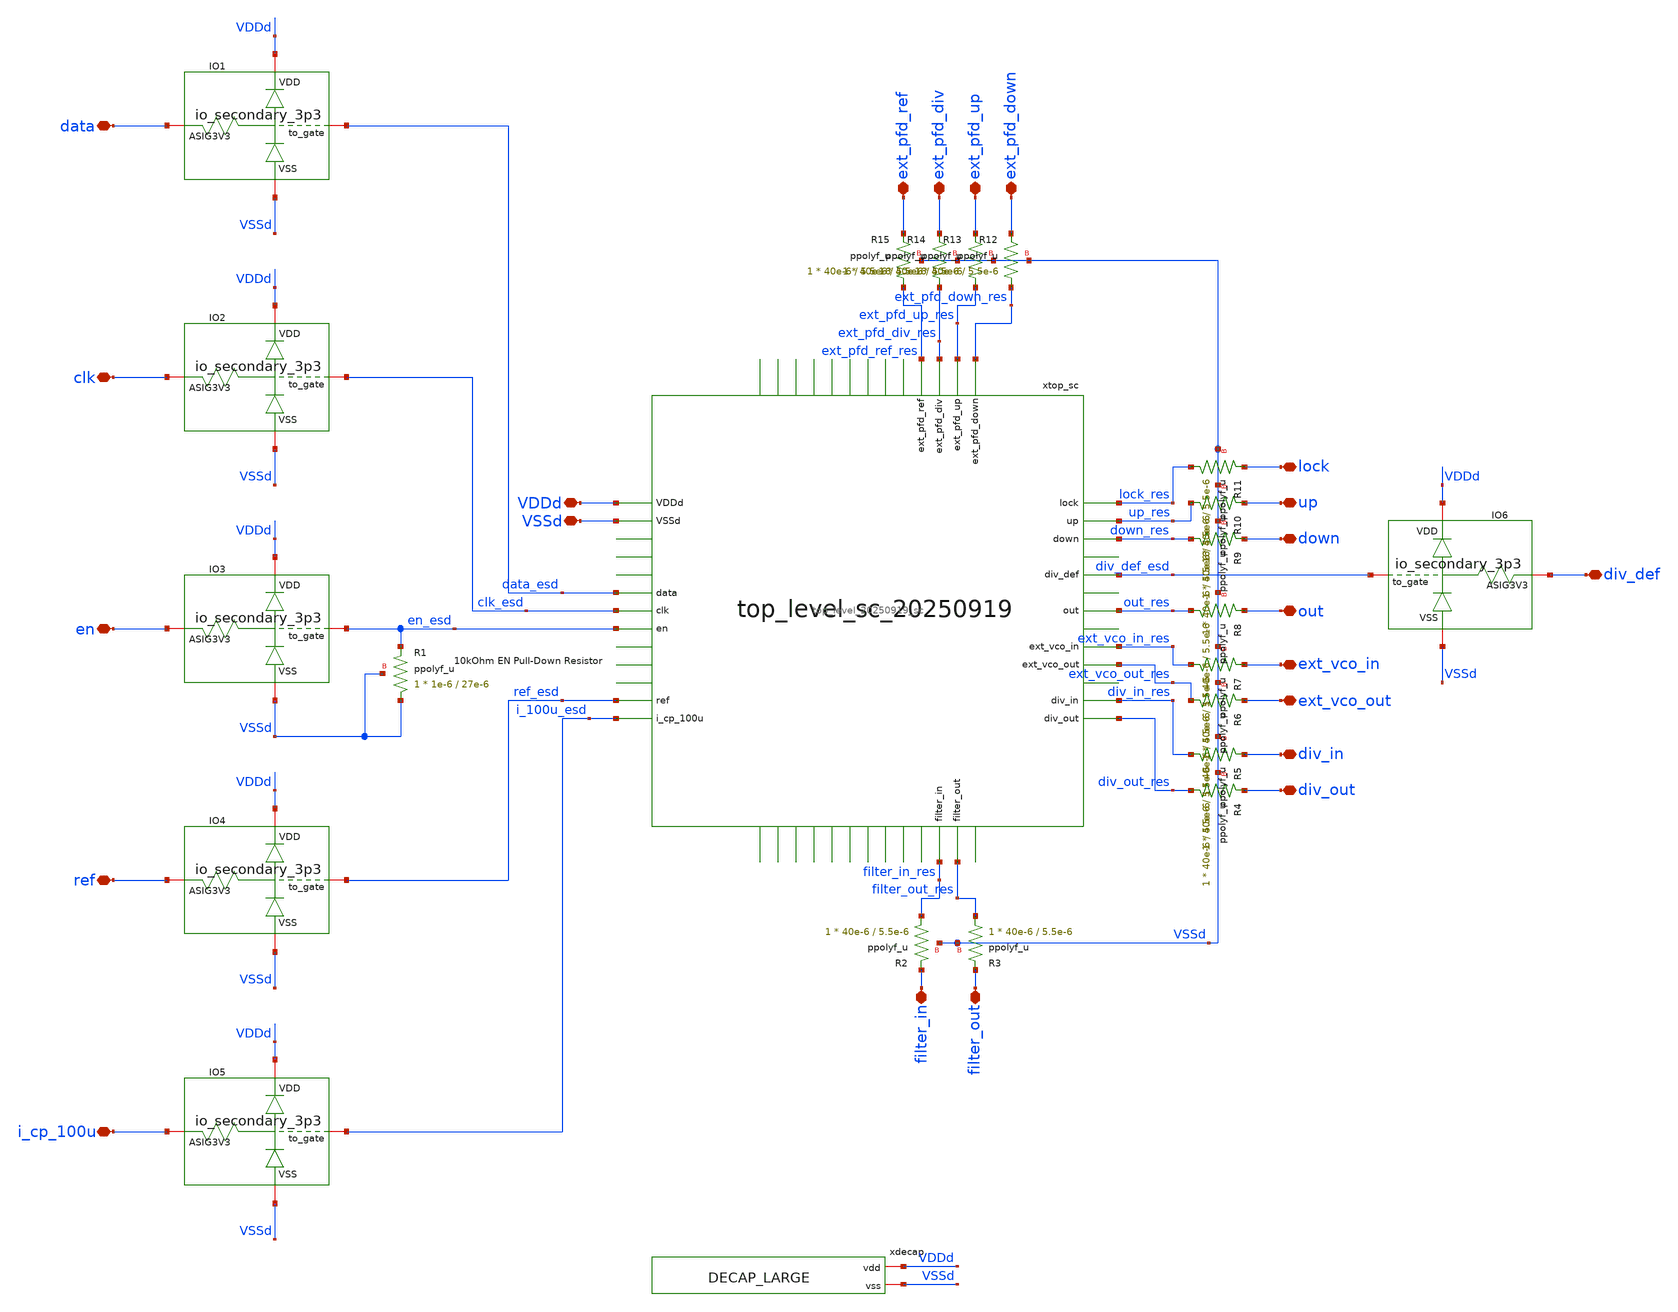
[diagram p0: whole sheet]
** sch_path: designs/libs/top_level/top_level_20250921/top_level_20250921.sch
**.subckt top_level_20250921 VDDd VSSd ref i_cp_100u filter_in filter_out ext_pfd_ref ext_pfd_up
*+ ext_pfd_down ext_pfd_div up down out lock ext_vco_out ext_vco_in div_out div_in data clk en div_def
*.iopin VDDd
*.iopin VSSd
*.iopin ref
*.iopin i_cp_100u
*.iopin filter_in
*.iopin filter_out
*.iopin ext_pfd_ref
*.iopin ext_pfd_up
*.iopin ext_pfd_down
*.iopin ext_pfd_div
*.iopin up
*.iopin down
*.iopin out
*.iopin lock
*.iopin ext_vco_out
*.iopin ext_vco_in
*.iopin div_out
*.iopin div_in
*.iopin data
*.iopin clk
*.iopin en
*.iopin div_def
xtop_sc VDDd VSSd data_esd clk_esd en_esd ref_esd i_100u_esd ext_pfd_ref_res ext_pfd_div_res
+ ext_pfd_up_res ext_pfd_down_res lock_res up_res down_res filter_out_res ext_vco_in_res div_in_res div_out_res
+ out_res filter_in_res ext_vco_out_res div_def_esd top_level_20250919_sc
XR1 VSSd en_esd VSSd ppolyf_u r_width=1e-6 r_length=27e-6 m=1
XIO1 VDDd data_esd data VSSd io_secondary_3p3
XIO2 VDDd clk_esd clk VSSd io_secondary_3p3
XIO3 VDDd en_esd en VSSd io_secondary_3p3
XIO4 VDDd ref_esd ref VSSd io_secondary_3p3
XIO5 VDDd i_100u_esd i_cp_100u VSSd io_secondary_3p3
XIO6 VDDd div_def_esd div_def VSSd io_secondary_3p3
xdecap VDDd VSSd DECAP_LARGE
XR2 filter_in_res filter_in VSSd ppolyf_u r_width=40e-6 r_length=5.5e-6 m=1
XR3 filter_out_res filter_out VSSd ppolyf_u r_width=40e-6 r_length=5.5e-6 m=1
XR4 div_out_res div_out VSSd ppolyf_u r_width=40e-6 r_length=5.5e-6 m=1
XR5 div_in_res div_in VSSd ppolyf_u r_width=40e-6 r_length=5.5e-6 m=1
XR6 ext_vco_out_res ext_vco_out VSSd ppolyf_u r_width=40e-6 r_length=5.5e-6 m=1
XR7 ext_vco_in_res ext_vco_in VSSd ppolyf_u r_width=40e-6 r_length=5.5e-6 m=1
XR8 out_res out VSSd ppolyf_u r_width=40e-6 r_length=5.5e-6 m=1
XR9 down_res down VSSd ppolyf_u r_width=40e-6 r_length=5.5e-6 m=1
XR10 up_res up VSSd ppolyf_u r_width=40e-6 r_length=5.5e-6 m=1
XR11 lock_res lock VSSd ppolyf_u r_width=40e-6 r_length=5.5e-6 m=1
XR12 ext_pfd_down_res ext_pfd_down VSSd ppolyf_u r_width=40e-6 r_length=5.5e-6 m=1
XR13 ext_pfd_up_res ext_pfd_up VSSd ppolyf_u r_width=40e-6 r_length=5.5e-6 m=1
XR14 ext_pfd_div_res ext_pfd_div VSSd ppolyf_u r_width=40e-6 r_length=5.5e-6 m=1
XR15 ext_pfd_ref_res ext_pfd_ref VSSd ppolyf_u r_width=40e-6 r_length=5.5e-6 m=1
**.ends
.end
